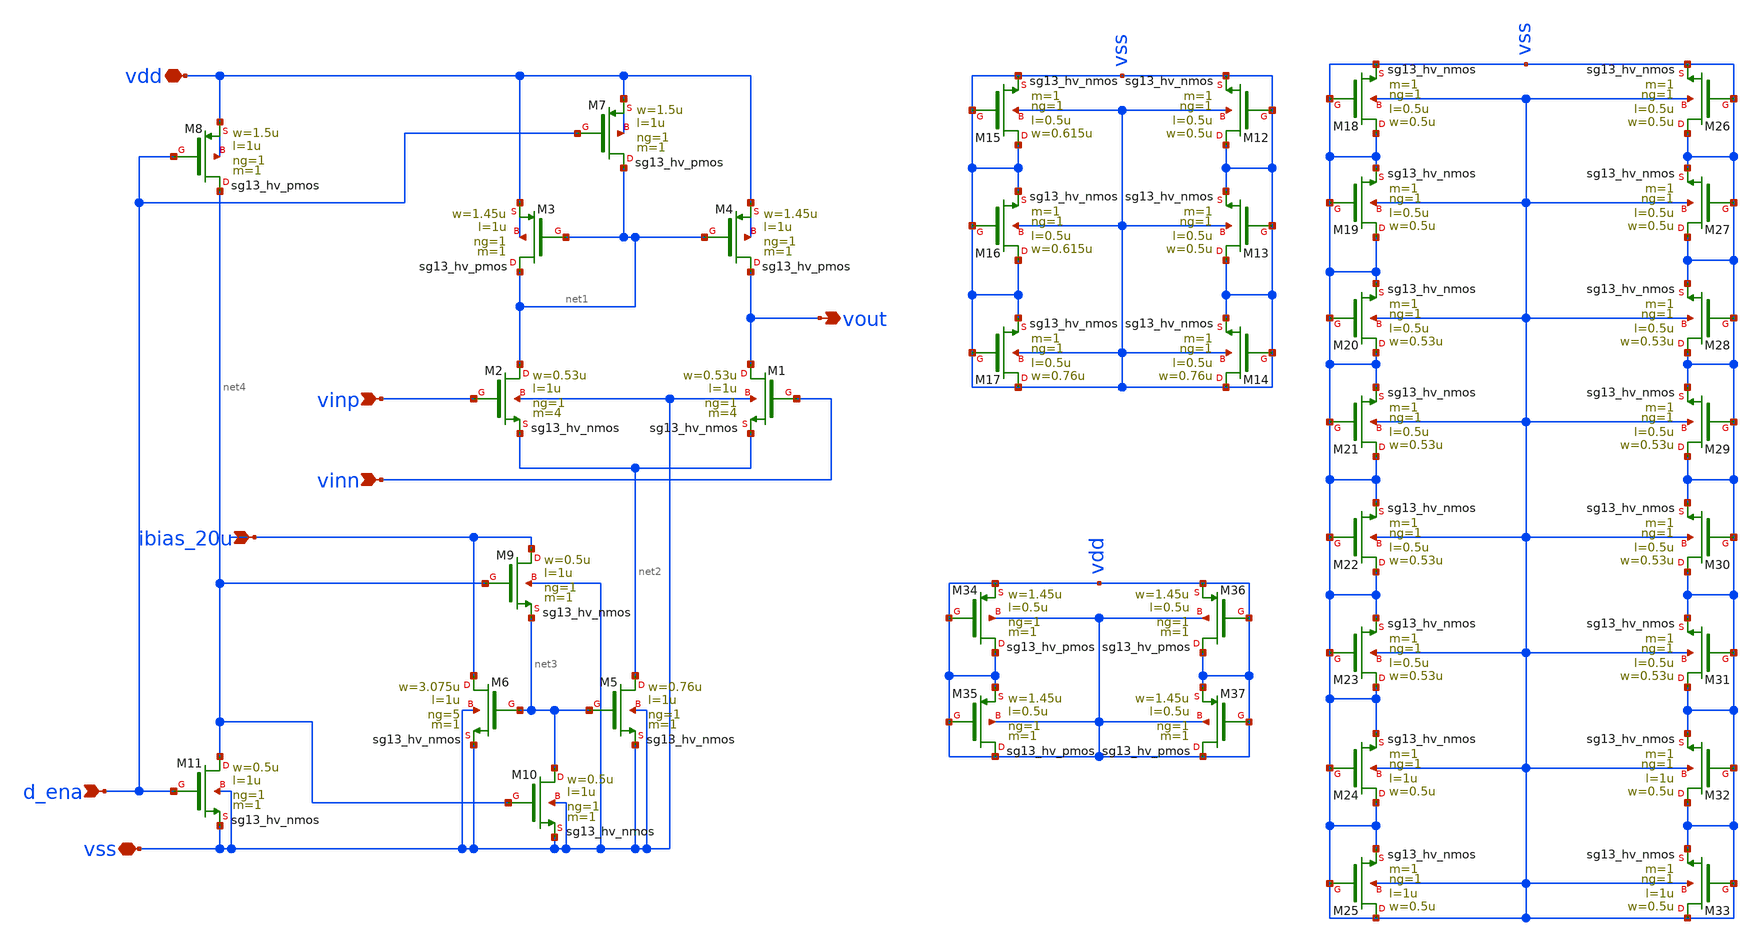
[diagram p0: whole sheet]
** sch_path: Differntial_Amp/design_data/xschem/ota.sch
**.subckt ota vout vdd vss ibias_20u vinn vinp d_ena
*.opin vout
*.iopin vdd
*.iopin vss
*.ipin ibias_20u
*.ipin vinn
*.ipin vinp
*.ipin d_ena
XM1 vout vinn net2 vss sg13_hv_nmos w=0.53u l=1u ng=1 m=4 mm_ok=1
XM2 net1 vinp net2 vss sg13_hv_nmos w=0.53u l=1u ng=1 m=4 mm_ok=1
XM5 net2 net3 vss vss sg13_hv_nmos w=0.76u l=1u ng=1 m=1 mm_ok=1
XM3 net1 net1 vdd vdd sg13_hv_pmos w=1.45u l=1u ng=1 m=1 mm_ok=1
XM4 vout net1 vdd vdd sg13_hv_pmos w=1.45u l=1u ng=1 m=1 mm_ok=1
XM6 ibias_20u net3 vss vss sg13_hv_nmos w=3.075u l=1u ng=5 m=1 mm_ok=1
XM7 net1 d_ena vdd vdd sg13_hv_pmos w=1.5u l=1u ng=1 m=1 mm_ok=1
XM8 net4 d_ena vdd vdd sg13_hv_pmos w=1.5u l=1u ng=1 m=1 mm_ok=1
XM9 ibias_20u net4 net3 vss sg13_hv_nmos w=0.5u l=1u ng=1 m=1 mm_ok=1
XM10 net3 net4 vss vss sg13_hv_nmos w=0.5u l=1u ng=1 m=1 mm_ok=1
XM11 net4 d_ena vss vss sg13_hv_nmos w=0.5u l=1u ng=1 m=1 mm_ok=1
XM12 vss vss vss vss sg13_hv_nmos w=0.5u l=0.5u ng=1 m=1 mm_ok=1
XM13 vss vss vss vss sg13_hv_nmos w=0.5u l=0.5u ng=1 m=1 mm_ok=1
XM14 vss vss vss vss sg13_hv_nmos w=0.76u l=0.5u ng=1 m=1 mm_ok=1
XM15 vss vss vss vss sg13_hv_nmos w=0.615u l=0.5u ng=1 m=1 mm_ok=1
XM16 vss vss vss vss sg13_hv_nmos w=0.615u l=0.5u ng=1 m=1 mm_ok=1
XM17 vss vss vss vss sg13_hv_nmos w=0.76u l=0.5u ng=1 m=1 mm_ok=1
XM18 vss vss vss vss sg13_hv_nmos w=0.5u l=0.5u ng=1 m=1 mm_ok=1
XM19 vss vss vss vss sg13_hv_nmos w=0.5u l=0.5u ng=1 m=1 mm_ok=1
XM20 vss vss vss vss sg13_hv_nmos w=0.53u l=0.5u ng=1 m=1 mm_ok=1
XM21 vss vss vss vss sg13_hv_nmos w=0.53u l=0.5u ng=1 m=1 mm_ok=1
XM22 vss vss vss vss sg13_hv_nmos w=0.53u l=0.5u ng=1 m=1 mm_ok=1
XM23 vss vss vss vss sg13_hv_nmos w=0.53u l=0.5u ng=1 m=1 mm_ok=1
XM24 vss vss vss vss sg13_hv_nmos w=0.5u l=1u ng=1 m=1 mm_ok=1
XM25 vss vss vss vss sg13_hv_nmos w=0.5u l=1u ng=1 m=1 mm_ok=1
XM26 vss vss vss vss sg13_hv_nmos w=0.5u l=0.5u ng=1 m=1 mm_ok=1
XM27 vss vss vss vss sg13_hv_nmos w=0.5u l=0.5u ng=1 m=1 mm_ok=1
XM28 vss vss vss vss sg13_hv_nmos w=0.53u l=0.5u ng=1 m=1 mm_ok=1
XM29 vss vss vss vss sg13_hv_nmos w=0.53u l=0.5u ng=1 m=1 mm_ok=1
XM30 vss vss vss vss sg13_hv_nmos w=0.53u l=0.5u ng=1 m=1 mm_ok=1
XM31 vss vss vss vss sg13_hv_nmos w=0.53u l=0.5u ng=1 m=1 mm_ok=1
XM32 vss vss vss vss sg13_hv_nmos w=0.5u l=1u ng=1 m=1 mm_ok=1
XM33 vss vss vss vss sg13_hv_nmos w=0.5u l=1u ng=1 m=1 mm_ok=1
XM34 vdd vdd vdd vdd sg13_hv_pmos w=1.45u l=0.5u ng=1 m=1 mm_ok=1
XM35 vdd vdd vdd vdd sg13_hv_pmos w=1.45u l=0.5u ng=1 m=1 mm_ok=1
XM36 vdd vdd vdd vdd sg13_hv_pmos w=1.45u l=0.5u ng=1 m=1 mm_ok=1
XM37 vdd vdd vdd vdd sg13_hv_pmos w=1.45u l=0.5u ng=1 m=1 mm_ok=1
**.ends
.end
